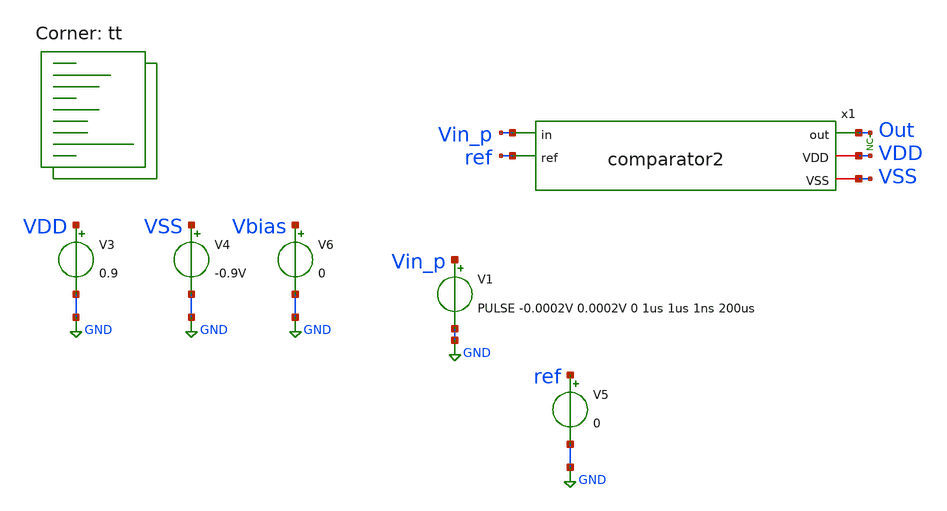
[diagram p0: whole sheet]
** sch_path: xschem/tests/comparator2/comparator2_test.sch
**.subckt comparator2_test
V3 VDD GND 0.9
V4 VSS GND -0.9V
V1 Vin_p GND PULSE -0.0002V 0.0002V 0 1us 1us 1ns 200us
V6 Vbias GND 0
V5 ref GND 0
x1 Out VDD VSS Vin_p ref comparator2
* noconn Out
**** begin user architecture code
 *.lib $::SKYWATER_MODELS/sky130.lib.spice tt
.include $::SKYWATER_STDCELLS/sky130_fd_sc_hd.spice



* Here's a comment
.options acct list
.options method=gear
.temp 25
*vvcc VDD 0 dc 1.8
*vvss VSS 0 0
.control
save all
tran 0.001u 2u
plot Vin_p 0.0002*out ref
plot i(v.x1.v1)
write comparator2_test.raw
.endc


.lib $::SKYWATER_MODELS/sky130.lib.spice tt
**** end user architecture code
**.ends

* expanding   symbol:  src/comparator2/comparator2.sym # of pins=5
** sym_path: xschem/src/comparator2/comparator2.sym
** sch_path: xschem/src/comparator2/comparator2.sch
.subckt comparator2 out VDD VSS in ref
*.iopin VDD
*.ipin in
*.opin out
*.iopin VSS
*.ipin ref
XM5 net5 net5 VDD VDD sky130_fd_pr__pfet_01v8 L=0.25 W=20 nf=4 ad='int((nf+1)/2) * W/nf * 0.29' as='int((nf+2)/2)
+ * W/nf * 0.29' pd='2*int((nf+1)/2) * (W/nf + 0.29)' ps='2*int((nf+2)/2) * (W/nf + 0.29)' nrd='0.29 /
+ W' nrs='0.29 / W' sa=0 sb=0 sd=0 mult=1 m=1
XM6 net4 net5 VDD VDD sky130_fd_pr__pfet_01v8 L=0.25 W=20 nf=4 ad='int((nf+1)/2) * W/nf * 0.29' as='int((nf+2)/2)
+ * W/nf * 0.29' pd='2*int((nf+1)/2) * (W/nf + 0.29)' ps='2*int((nf+2)/2) * (W/nf + 0.29)' nrd='0.29 /
+ W' nrs='0.29 / W' sa=0 sb=0 sd=0 mult=1 m=1
XM10 net1 net2 VSS VSS sky130_fd_pr__nfet_01v8 L=0.25 W=15 nf=4 ad='int((nf+1)/2) * W/nf * 0.29' as='int((nf+2)/2)
+ * W/nf * 0.29' pd='2*int((nf+1)/2) * (W/nf + 0.29)' ps='2*int((nf+2)/2) * (W/nf + 0.29)' nrd='0.29 /
+ W' nrs='0.29 / W' sa=0 sb=0 sd=0 mult=1 m=1
XM11 VSS net2 net2 VSS sky130_fd_pr__nfet_01v8 L=2 W=20 nf=4 ad='int((nf+1)/2) * W/nf * 0.29' as='int((nf+2)/2)
+ * W/nf * 0.29' pd='2*int((nf+1)/2) * (W/nf + 0.29)' ps='2*int((nf+2)/2) * (W/nf + 0.29)' nrd='0.29 /
+ W' nrs='0.29 / W' sa=0 sb=0 sd=0 mult=1 m=1
XM12 net3 net2 VSS VSS sky130_fd_pr__nfet_01v8 L=1.05 W=3 nf=4 ad='int((nf+1)/2) * W/nf * 0.29' as='int((nf+2)/2)
+ * W/nf * 0.29' pd='2*int((nf+1)/2) * (W/nf + 0.29)' ps='2*int((nf+2)/2) * (W/nf + 0.29)' nrd='0.29 /
+ W' nrs='0.29 / W' sa=0 sb=0 sd=0 mult=1 m=1
XM13 out net3 VDD VDD sky130_fd_pr__pfet_01v8 L=0.5 W=2 nf=1 ad='int((nf+1)/2) * W/nf * 0.29' as='int((nf+2)/2)
+ * W/nf * 0.29' pd='2*int((nf+1)/2) * (W/nf + 0.29)' ps='2*int((nf+2)/2) * (W/nf + 0.29)' nrd='0.29 /
+ W' nrs='0.29 / W' sa=0 sb=0 sd=0 mult=1 m=1
XM14 out net3 VSS VSS sky130_fd_pr__nfet_01v8 L=0.5 W=2 nf=1 ad='int((nf+1)/2) * W/nf * 0.29' as='int((nf+2)/2)
+ * W/nf * 0.29' pd='2*int((nf+1)/2) * (W/nf + 0.29)' ps='2*int((nf+2)/2) * (W/nf + 0.29)' nrd='0.29 /
+ W' nrs='0.29 / W' sa=0 sb=0 sd=0 mult=1 m=1
XM2 net3 net4 VDD VDD sky130_fd_pr__pfet_01v8 L=0.3 W=19 nf=1 ad='int((nf+1)/2) * W/nf * 0.29' as='int((nf+2)/2)
+ * W/nf * 0.29' pd='2*int((nf+1)/2) * (W/nf + 0.29)' ps='2*int((nf+2)/2) * (W/nf + 0.29)' nrd='0.29 /
+ W' nrs='0.29 / W' sa=0 sb=0 sd=0 mult=1 m=1
XM1 net5 in net1 VSS sky130_fd_pr__nfet_01v8 L=1 W=20 nf=4 ad='int((nf+1)/2) * W/nf * 0.29' as='int((nf+2)/2)
+ * W/nf * 0.29' pd='2*int((nf+1)/2) * (W/nf + 0.29)' ps='2*int((nf+2)/2) * (W/nf + 0.29)' nrd='0.29 /
+ W' nrs='0.29 / W' sa=0 sb=0 sd=0 mult=1 m=1
XM3 net4 ref net1 VSS sky130_fd_pr__nfet_01v8 L=1 W=20 nf=4 ad='int((nf+1)/2) * W/nf * 0.29' as='int((nf+2)/2)
+ * W/nf * 0.29' pd='2*int((nf+1)/2) * (W/nf + 0.29)' ps='2*int((nf+2)/2) * (W/nf + 0.29)' nrd='0.29 /
+ W' nrs='0.29 / W' sa=0 sb=0 sd=0 mult=1 m=1
XR1 net6 VDD VSS sky130_fd_pr__res_high_po_0p35 L=25 mult=0.5 m=0.5
V1 net6 net2 0
.ends

.GLOBAL GND
.end
